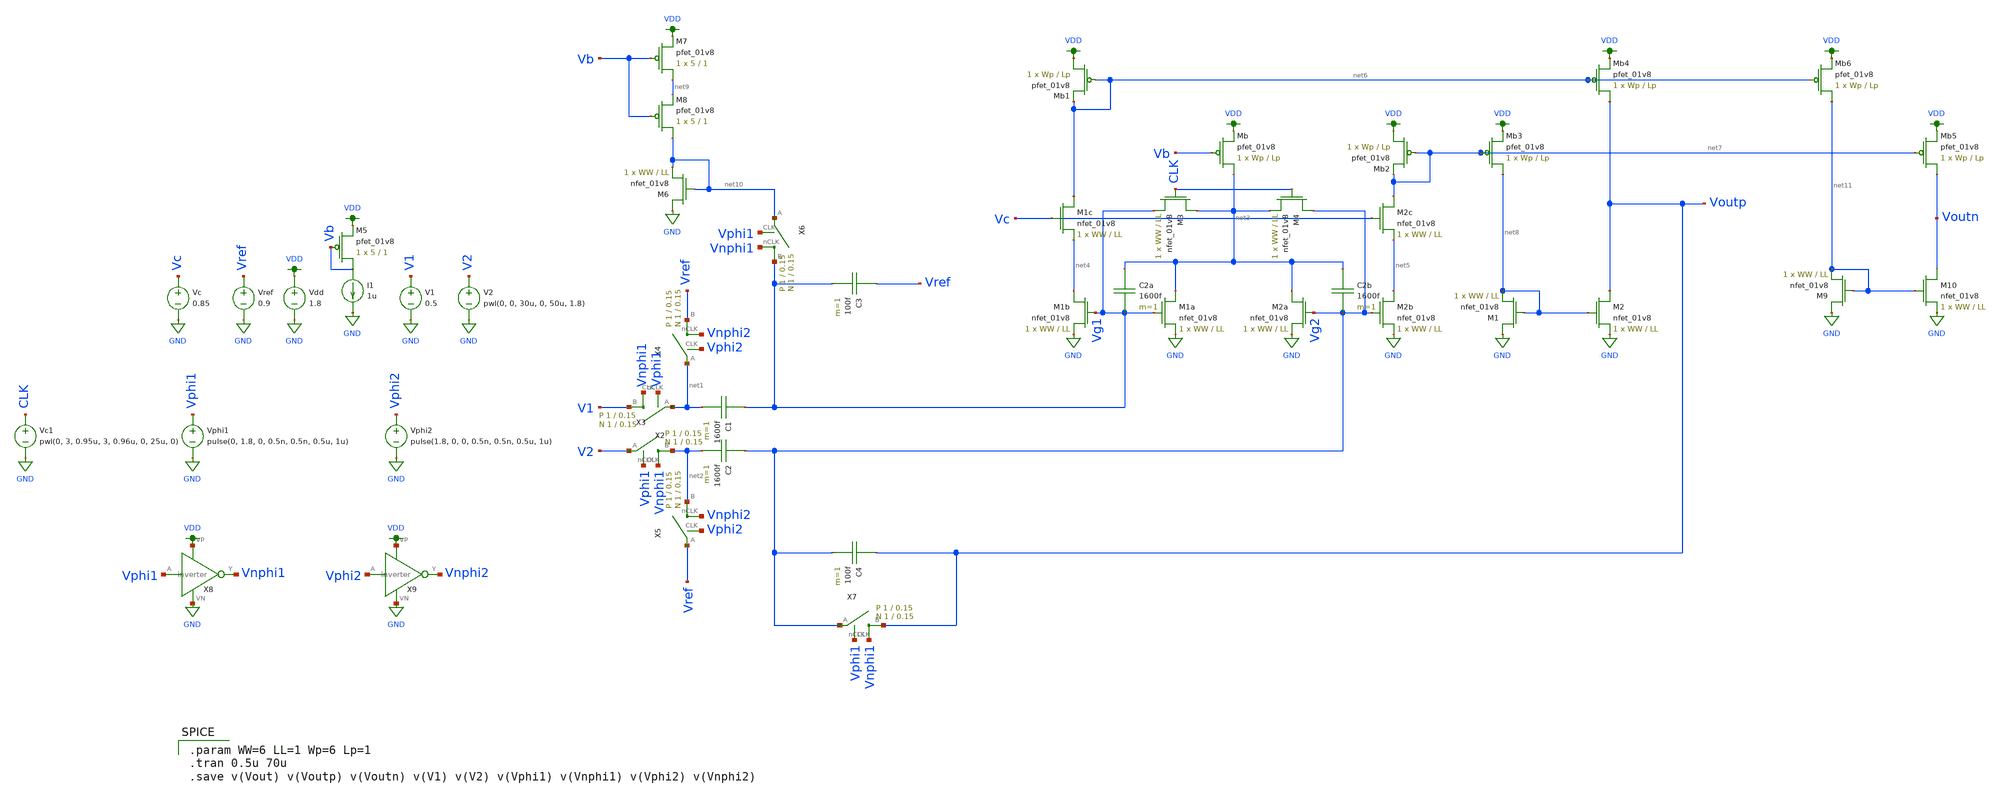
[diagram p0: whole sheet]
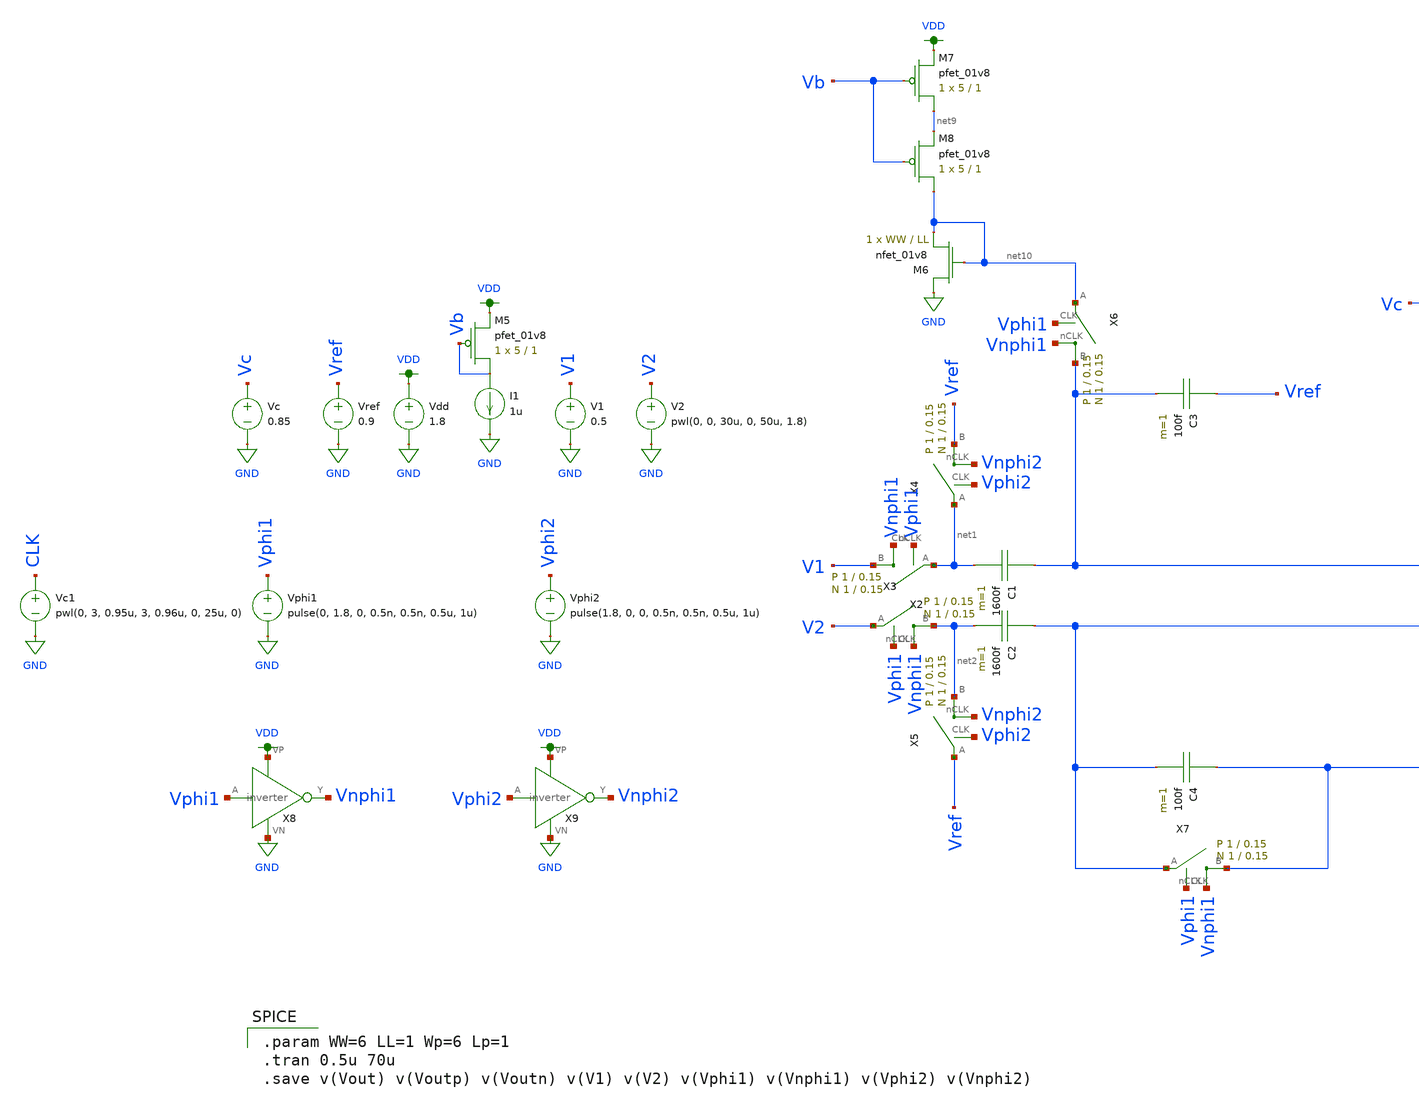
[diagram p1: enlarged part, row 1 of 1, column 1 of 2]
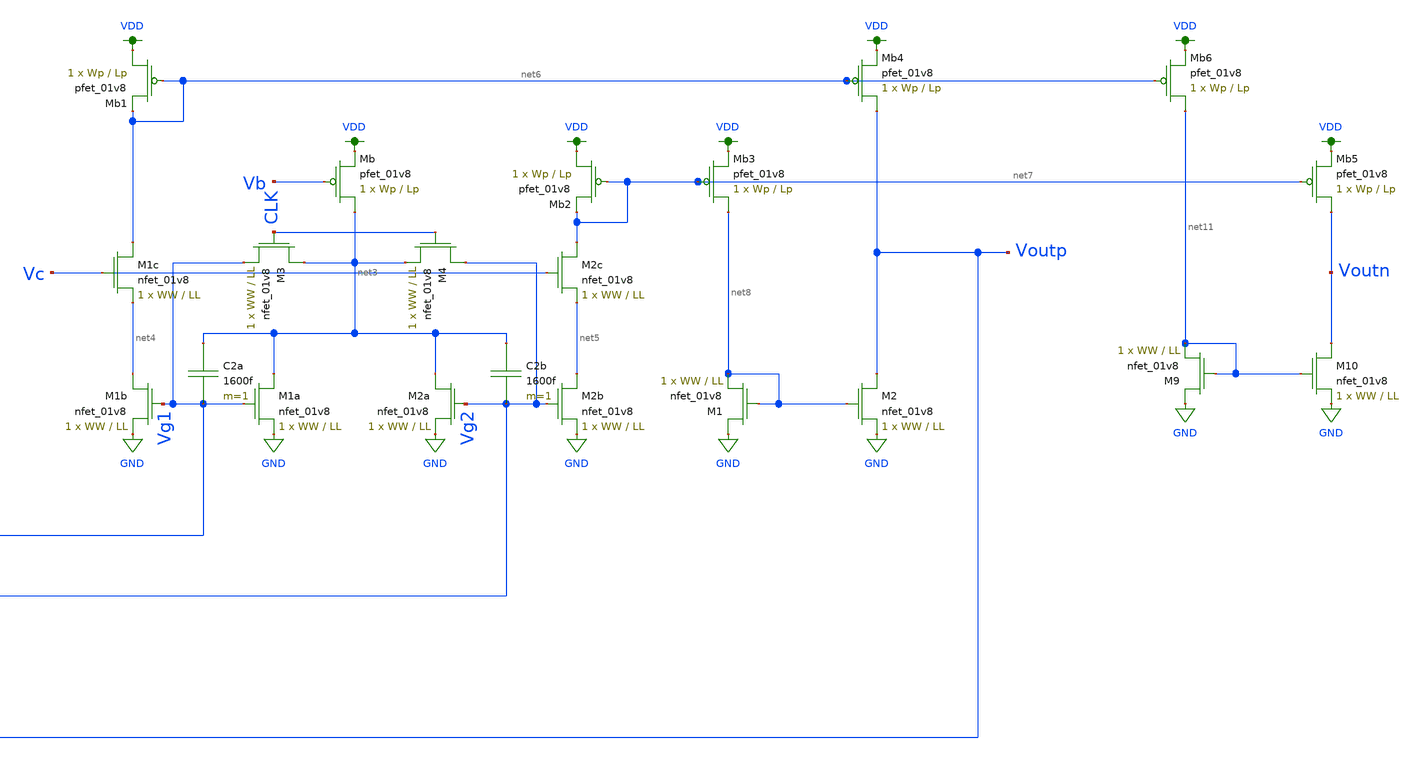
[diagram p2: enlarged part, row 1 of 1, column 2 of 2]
** sch_path: schematic/alpha_amp_fancy.sch
**.subckt alpha_amp_fancy
C1 Vg1 net1 1600f m=1
C2 Vg2 net2 1600f m=1
C3 Vref Vg1 100f m=1
C4 Voutp Vg2 100f m=1
X2 V1 net1 Vphi1 Vnphi1 switch Wp=1 Lp=0.15 WW=1 LL=0.15
X3 net2 V2 Vphi1 Vnphi1 switch Wp=1 Lp=0.15 WW=1 LL=0.15
X4 Vref net1 Vphi2 Vnphi2 switch Wp=1 Lp=0.15 WW=1 LL=0.15
X5 net2 Vref Vphi2 Vnphi2 switch Wp=1 Lp=0.15 WW=1 LL=0.15
X6 Vg1 net10 Vphi1 Vnphi1 switch Wp=1 Lp=0.15 WW=1 LL=0.15
X7 Voutp Vg2 Vphi1 Vnphi1 switch Wp=1 Lp=0.15 WW=1 LL=0.15
Vdd VDD GND 1.8
V1 V1 GND 0.5
V2 V2 GND pwl(0, 0, 30u, 0, 50u, 1.8)
Vphi1 Vphi1 GND pulse(0, 1.8, 0, 0.5n, 0.5n, 0.5u, 1u)
X8 Vphi1 Vnphi1 VDD GND inverter
Vphi2 Vphi2 GND pulse(1.8, 0, 0, 0.5n, 0.5n, 0.5u, 1u)
X9 Vphi2 Vnphi2 VDD GND inverter
Vref Vref GND 0.9
XM1a net3 Vg1 GND GND sky130_fd_pr__nfet_01v8 L=LL W=WW nf=1 ad='int((nf+1)/2) * W/nf * 0.29' as='int((nf+2)/2) * W/nf * 0.29'
+ pd='2*int((nf+1)/2) * (W/nf + 0.29)' ps='2*int((nf+2)/2) * (W/nf + 0.29)' nrd='0.29 / W' nrs='0.29 / W'
+ sa=0 sb=0 sd=0 mult=1 m=1
XM1b net4 Vg1 GND GND sky130_fd_pr__nfet_01v8 L=LL W=WW nf=1 ad='int((nf+1)/2) * W/nf * 0.29' as='int((nf+2)/2) * W/nf * 0.29'
+ pd='2*int((nf+1)/2) * (W/nf + 0.29)' ps='2*int((nf+2)/2) * (W/nf + 0.29)' nrd='0.29 / W' nrs='0.29 / W'
+ sa=0 sb=0 sd=0 mult=1 m=1
XM1c net6 Vc net4 GND sky130_fd_pr__nfet_01v8 L=LL W=WW nf=1 ad='int((nf+1)/2) * W/nf * 0.29' as='int((nf+2)/2) * W/nf * 0.29'
+ pd='2*int((nf+1)/2) * (W/nf + 0.29)' ps='2*int((nf+2)/2) * (W/nf + 0.29)' nrd='0.29 / W' nrs='0.29 / W'
+ sa=0 sb=0 sd=0 mult=1 m=1
XM2b net5 Vg2 GND GND sky130_fd_pr__nfet_01v8 L=LL W=WW nf=1 ad='int((nf+1)/2) * W/nf * 0.29' as='int((nf+2)/2) * W/nf * 0.29'
+ pd='2*int((nf+1)/2) * (W/nf + 0.29)' ps='2*int((nf+2)/2) * (W/nf + 0.29)' nrd='0.29 / W' nrs='0.29 / W'
+ sa=0 sb=0 sd=0 mult=1 m=1
XM2a net3 Vg2 GND GND sky130_fd_pr__nfet_01v8 L=LL W=WW nf=1 ad='int((nf+1)/2) * W/nf * 0.29' as='int((nf+2)/2) * W/nf * 0.29'
+ pd='2*int((nf+1)/2) * (W/nf + 0.29)' ps='2*int((nf+2)/2) * (W/nf + 0.29)' nrd='0.29 / W' nrs='0.29 / W'
+ sa=0 sb=0 sd=0 mult=1 m=1
XM2c net7 Vc net5 GND sky130_fd_pr__nfet_01v8 L=LL W=WW nf=1 ad='int((nf+1)/2) * W/nf * 0.29' as='int((nf+2)/2) * W/nf * 0.29'
+ pd='2*int((nf+1)/2) * (W/nf + 0.29)' ps='2*int((nf+2)/2) * (W/nf + 0.29)' nrd='0.29 / W' nrs='0.29 / W'
+ sa=0 sb=0 sd=0 mult=1 m=1
XMb net3 Vb VDD VDD sky130_fd_pr__pfet_01v8 L=Lp W=Wp nf=1 ad='int((nf+1)/2) * W/nf * 0.29' as='int((nf+2)/2) * W/nf * 0.29'
+ pd='2*int((nf+1)/2) * (W/nf + 0.29)' ps='2*int((nf+2)/2) * (W/nf + 0.29)' nrd='0.29 / W' nrs='0.29 / W'
+ sa=0 sb=0 sd=0 mult=1 m=1
C2b net3 Vg2 1600f m=1
C2a net3 Vg1 1600f m=1
Vc Vc GND 0.85
XMb1 VDD net6 net6 VDD sky130_fd_pr__pfet_01v8 L=Lp W=Wp nf=1 ad='int((nf+1)/2) * W/nf * 0.29' as='int((nf+2)/2) * W/nf * 0.29'
+ pd='2*int((nf+1)/2) * (W/nf + 0.29)' ps='2*int((nf+2)/2) * (W/nf + 0.29)' nrd='0.29 / W' nrs='0.29 / W'
+ sa=0 sb=0 sd=0 mult=1 m=1
XMb2 VDD net7 net7 VDD sky130_fd_pr__pfet_01v8 L=Lp W=Wp nf=1 ad='int((nf+1)/2) * W/nf * 0.29' as='int((nf+2)/2) * W/nf * 0.29'
+ pd='2*int((nf+1)/2) * (W/nf + 0.29)' ps='2*int((nf+2)/2) * (W/nf + 0.29)' nrd='0.29 / W' nrs='0.29 / W'
+ sa=0 sb=0 sd=0 mult=1 m=1
XMb3 net8 net7 VDD VDD sky130_fd_pr__pfet_01v8 L=Lp W=Wp nf=1 ad='int((nf+1)/2) * W/nf * 0.29' as='int((nf+2)/2) * W/nf * 0.29'
+ pd='2*int((nf+1)/2) * (W/nf + 0.29)' ps='2*int((nf+2)/2) * (W/nf + 0.29)' nrd='0.29 / W' nrs='0.29 / W'
+ sa=0 sb=0 sd=0 mult=1 m=1
XM1 GND net8 net8 GND sky130_fd_pr__nfet_01v8 L=LL W=WW nf=1 ad='int((nf+1)/2) * W/nf * 0.29' as='int((nf+2)/2) * W/nf * 0.29'
+ pd='2*int((nf+1)/2) * (W/nf + 0.29)' ps='2*int((nf+2)/2) * (W/nf + 0.29)' nrd='0.29 / W' nrs='0.29 / W'
+ sa=0 sb=0 sd=0 mult=1 m=1
XMb4 Voutp net6 VDD VDD sky130_fd_pr__pfet_01v8 L=Lp W=Wp nf=1 ad='int((nf+1)/2) * W/nf * 0.29' as='int((nf+2)/2) * W/nf * 0.29'
+ pd='2*int((nf+1)/2) * (W/nf + 0.29)' ps='2*int((nf+2)/2) * (W/nf + 0.29)' nrd='0.29 / W' nrs='0.29 / W'
+ sa=0 sb=0 sd=0 mult=1 m=1
XM2 Voutp net8 GND GND sky130_fd_pr__nfet_01v8 L=LL W=WW nf=1 ad='int((nf+1)/2) * W/nf * 0.29' as='int((nf+2)/2) * W/nf * 0.29'
+ pd='2*int((nf+1)/2) * (W/nf + 0.29)' ps='2*int((nf+2)/2) * (W/nf + 0.29)' nrd='0.29 / W' nrs='0.29 / W'
+ sa=0 sb=0 sd=0 mult=1 m=1
XM3 net3 CLK Vg1 GND sky130_fd_pr__nfet_01v8 L=LL W=WW nf=1 ad='int((nf+1)/2) * W/nf * 0.29' as='int((nf+2)/2) * W/nf * 0.29'
+ pd='2*int((nf+1)/2) * (W/nf + 0.29)' ps='2*int((nf+2)/2) * (W/nf + 0.29)' nrd='0.29 / W' nrs='0.29 / W'
+ sa=0 sb=0 sd=0 mult=1 m=1
XM4 Vg2 CLK net3 GND sky130_fd_pr__nfet_01v8 L=LL W=WW nf=1 ad='int((nf+1)/2) * W/nf * 0.29' as='int((nf+2)/2) * W/nf * 0.29'
+ pd='2*int((nf+1)/2) * (W/nf + 0.29)' ps='2*int((nf+2)/2) * (W/nf + 0.29)' nrd='0.29 / W' nrs='0.29 / W'
+ sa=0 sb=0 sd=0 mult=1 m=1
Vc1 CLK GND pwl(0, 3, 0.95u, 3, 0.96u, 0, 25u, 0)
XM5 Vb Vb VDD VDD sky130_fd_pr__pfet_01v8 L=1 W=5 nf=1 ad='int((nf+1)/2) * W/nf * 0.29' as='int((nf+2)/2) * W/nf * 0.29'
+ pd='2*int((nf+1)/2) * (W/nf + 0.29)' ps='2*int((nf+2)/2) * (W/nf + 0.29)' nrd='0.29 / W' nrs='0.29 / W'
+ sa=0 sb=0 sd=0 mult=1 m=1
I1 Vb GND 1u
XM7 net9 Vb VDD VDD sky130_fd_pr__pfet_01v8 L=1 W=5 nf=1 ad='int((nf+1)/2) * W/nf * 0.29' as='int((nf+2)/2) * W/nf * 0.29'
+ pd='2*int((nf+1)/2) * (W/nf + 0.29)' ps='2*int((nf+2)/2) * (W/nf + 0.29)' nrd='0.29 / W' nrs='0.29 / W'
+ sa=0 sb=0 sd=0 mult=1 m=1
XM8 net10 Vb net9 VDD sky130_fd_pr__pfet_01v8 L=1 W=5 nf=1 ad='int((nf+1)/2) * W/nf * 0.29' as='int((nf+2)/2) * W/nf * 0.29'
+ pd='2*int((nf+1)/2) * (W/nf + 0.29)' ps='2*int((nf+2)/2) * (W/nf + 0.29)' nrd='0.29 / W' nrs='0.29 / W'
+ sa=0 sb=0 sd=0 mult=1 m=1
XM6 GND net10 net10 GND sky130_fd_pr__nfet_01v8 L=LL W=WW nf=1 ad='int((nf+1)/2) * W/nf * 0.29' as='int((nf+2)/2) * W/nf * 0.29'
+ pd='2*int((nf+1)/2) * (W/nf + 0.29)' ps='2*int((nf+2)/2) * (W/nf + 0.29)' nrd='0.29 / W' nrs='0.29 / W'
+ sa=0 sb=0 sd=0 mult=1 m=1
XMb5 Voutn net7 VDD VDD sky130_fd_pr__pfet_01v8 L=Lp W=Wp nf=1 ad='int((nf+1)/2) * W/nf * 0.29' as='int((nf+2)/2) * W/nf * 0.29'
+ pd='2*int((nf+1)/2) * (W/nf + 0.29)' ps='2*int((nf+2)/2) * (W/nf + 0.29)' nrd='0.29 / W' nrs='0.29 / W'
+ sa=0 sb=0 sd=0 mult=1 m=1
XMb6 net11 net6 VDD VDD sky130_fd_pr__pfet_01v8 L=Lp W=Wp nf=1 ad='int((nf+1)/2) * W/nf * 0.29' as='int((nf+2)/2) * W/nf * 0.29'
+ pd='2*int((nf+1)/2) * (W/nf + 0.29)' ps='2*int((nf+2)/2) * (W/nf + 0.29)' nrd='0.29 / W' nrs='0.29 / W'
+ sa=0 sb=0 sd=0 mult=1 m=1
XM9 GND net11 net11 GND sky130_fd_pr__nfet_01v8 L=LL W=WW nf=1 ad='int((nf+1)/2) * W/nf * 0.29' as='int((nf+2)/2) * W/nf * 0.29'
+ pd='2*int((nf+1)/2) * (W/nf + 0.29)' ps='2*int((nf+2)/2) * (W/nf + 0.29)' nrd='0.29 / W' nrs='0.29 / W'
+ sa=0 sb=0 sd=0 mult=1 m=1
XM10 Voutn net11 GND GND sky130_fd_pr__nfet_01v8 L=LL W=WW nf=1 ad='int((nf+1)/2) * W/nf * 0.29' as='int((nf+2)/2) * W/nf * 0.29'
+ pd='2*int((nf+1)/2) * (W/nf + 0.29)' ps='2*int((nf+2)/2) * (W/nf + 0.29)' nrd='0.29 / W' nrs='0.29 / W'
+ sa=0 sb=0 sd=0 mult=1 m=1
**** begin user architecture code

.option wnflag=1
.param MC_SWITCH=0.0
.lib ~/skywater/skywater-pdk/libraries/sky130_fd_pr_ngspice/latest/models/sky130.lib.spice tt


.param WW=6 LL=1 Wp=6 Lp=1
.tran 0.5u 70u
.save v(Vout) v(Voutp) v(Voutn) v(V1) v(V2) v(Vphi1) v(Vnphi1) v(Vphi2) v(Vnphi2)

**** end user architecture code
**.ends

* expanding   symbol:  /home/madvlsi/Documents/MADVLSI-Final_Project/schematic/switch.sym # of
*+ pins=4
** sym_path: schematic/switch.sym
** sch_path: schematic/switch.sch
.subckt switch B A CLK nCLK  Wp=1 Lp=0.15 WW=1 LL=0.15
*.iopin B
*.iopin A
*.ipin CLK
*.ipin nCLK
*.ipin CLK
*.ipin CLK
*.ipin nCLK
*.ipin nCLK
XM1 A CLK B GND sky130_fd_pr__nfet_01v8 L={LL} W={WW} nf=1 ad='int((nf+1)/2) * W/nf * 0.29' as='int((nf+2)/2) * W/nf * 0.29'
+ pd='2*int((nf+1)/2) * (W/nf + 0.29)' ps='2*int((nf+2)/2) * (W/nf + 0.29)' nrd='0.29 / W' nrs='0.29 / W'
+ sa=0 sb=0 sd=0 mult=1 m=1
XM2 A nCLK B VDD sky130_fd_pr__pfet_01v8 L={Lp} W={Wp} nf=1 ad='int((nf+1)/2) * W/nf * 0.29' as='int((nf+2)/2) * W/nf * 0.29'
+ pd='2*int((nf+1)/2) * (W/nf + 0.29)' ps='2*int((nf+2)/2) * (W/nf + 0.29)' nrd='0.29 / W' nrs='0.29 / W'
+ sa=0 sb=0 sd=0 mult=1 m=1
XM3 B CLK B VDD sky130_fd_pr__pfet_01v8 L={Lp} W={Wp/2} nf=1 ad='int((nf+1)/2) * W/nf * 0.29' as='int((nf+2)/2) * W/nf * 0.29'
+ pd='2*int((nf+1)/2) * (W/nf + 0.29)' ps='2*int((nf+2)/2) * (W/nf + 0.29)' nrd='0.29 / W' nrs='0.29 / W'
+ sa=0 sb=0 sd=0 mult=1 m=1
XM4 A CLK A VDD sky130_fd_pr__pfet_01v8 L={Lp} W={Wp/2} nf=1 ad='int((nf+1)/2) * W/nf * 0.29' as='int((nf+2)/2) * W/nf * 0.29'
+ pd='2*int((nf+1)/2) * (W/nf + 0.29)' ps='2*int((nf+2)/2) * (W/nf + 0.29)' nrd='0.29 / W' nrs='0.29 / W'
+ sa=0 sb=0 sd=0 mult=1 m=1
XM5 B nCLK B GND sky130_fd_pr__nfet_01v8 L={LL} W={WW/2} nf=1 ad='int((nf+1)/2) * W/nf * 0.29' as='int((nf+2)/2) * W/nf * 0.29'
+ pd='2*int((nf+1)/2) * (W/nf + 0.29)' ps='2*int((nf+2)/2) * (W/nf + 0.29)' nrd='0.29 / W' nrs='0.29 / W'
+ sa=0 sb=0 sd=0 mult=1 m=1
XM6 A nCLK A GND sky130_fd_pr__nfet_01v8 L={LL} W={WW/2} nf=1 ad='int((nf+1)/2) * W/nf * 0.29' as='int((nf+2)/2) * W/nf * 0.29'
+ pd='2*int((nf+1)/2) * (W/nf + 0.29)' ps='2*int((nf+2)/2) * (W/nf + 0.29)' nrd='0.29 / W' nrs='0.29 / W'
+ sa=0 sb=0 sd=0 mult=1 m=1
.ends


* expanding   symbol:  /home/madvlsi/Documents/MADVLSI-Final_Project/schematic/inverter.sym # of
*+ pins=4
** sym_path: schematic/inverter.sym
** sch_path: schematic/inverter.sch
.subckt inverter A Y VP VN
*.opin Y
*.ipin A
*.iopin VP
*.iopin VN
XM3 Y A VP VDD sky130_fd_pr__pfet_01v8 L={Lp} W={Wp} nf=1 ad='int((nf+1)/2) * W/nf * 0.29' as='int((nf+2)/2) * W/nf * 0.29'
+ pd='2*int((nf+1)/2) * (W/nf + 0.29)' ps='2*int((nf+2)/2) * (W/nf + 0.29)' nrd='0.29 / W' nrs='0.29 / W'
+ sa=0 sb=0 sd=0 mult=1 m=1
XM4 Y A VP VDD sky130_fd_pr__pfet_01v8 L={Lp} W={Wp} nf=1 ad='int((nf+1)/2) * W/nf * 0.29' as='int((nf+2)/2) * W/nf * 0.29'
+ pd='2*int((nf+1)/2) * (W/nf + 0.29)' ps='2*int((nf+2)/2) * (W/nf + 0.29)' nrd='0.29 / W' nrs='0.29 / W'
+ sa=0 sb=0 sd=0 mult=1 m=1
XM5 Y A VN GND sky130_fd_pr__nfet_01v8 L={Lp} W={Wp} nf=1 ad='int((nf+1)/2) * W/nf * 0.29' as='int((nf+2)/2) * W/nf * 0.29'
+ pd='2*int((nf+1)/2) * (W/nf + 0.29)' ps='2*int((nf+2)/2) * (W/nf + 0.29)' nrd='0.29 / W' nrs='0.29 / W'
+ sa=0 sb=0 sd=0 mult=1 m=1
.ends

.GLOBAL GND
.GLOBAL VDD
.end
